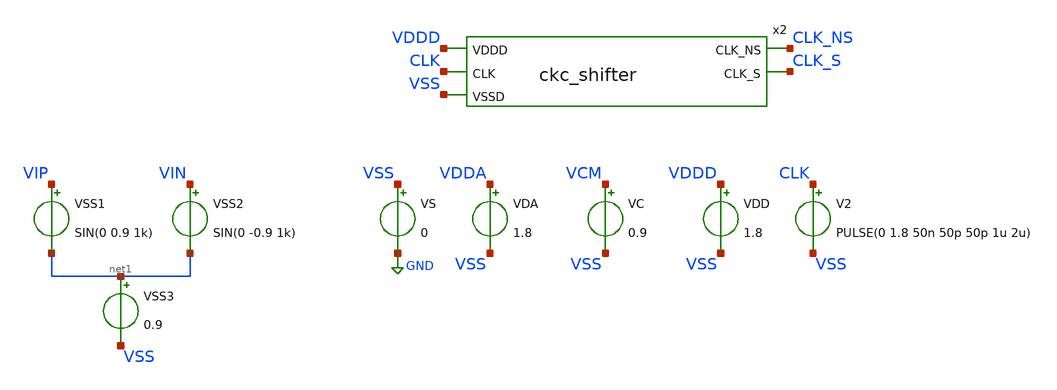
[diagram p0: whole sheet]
** sch_path: xschem/untitled.sch
**.subckt untitled
x2 VDDD CLK VSS CLK_NS CLK_S ckc_shifter
VS VSS GND 0
VDA VDDA VSS 1.8
VDD VDDD VSS 1.8
VC VCM VSS 0.9
VSS1 VIP net1 SIN(0 0.9 1k)
VSS2 VIN net1 SIN(0 -0.9 1k)
VSS3 net1 VSS 0.9
V2 CLK VSS PULSE(0 1.8 50n 50p 50p 1u 2u)
**** begin user architecture code

** opencircuitdesign pdks install
.lib $::SKYWATER_MODELS/sky130.lib.spice tt
.include /usr/local/share/pdk/sky130A/libs.ref/sky130_fd_sc_hd/spice/sky130_fd_sc_hd.spice



.option wnflag=0
.option savecurrents
.control
tran 1n 1m
plot DOUT[0:3]
.endc

**** end user architecture code
**.ends

* expanding   symbol:  ckc_shifter.sym # of pins=5
** sym_path: ckc_shifter.sym
** sch_path: ckc_shifter.sch
.subckt ckc_shifter VDDD CLK VSSD CLK_NS CLK_S
*.ipin CLK
*.ipin VDDD
*.ipin VSSD
*.opin CLK_NS
*.opin CLK_S
x1 CLK FB0 VDDD VSSD VSSD VDDD VDDD CLK_1 FB0 sky130_fd_sc_hd__dfrbp_2
x2 CLK_1 CLK_S VDDD VSSD VSSD VDDD VDDD net1 CLK_S sky130_fd_sc_hd__dfrbp_2
* noconn #net1
x3 CLK_1 FB1 VDDD VSSD VSSD VDDD VDDD CLK_NS FB1 sky130_fd_sc_hd__dfrbp_2
.ends

.GLOBAL GND
.end
